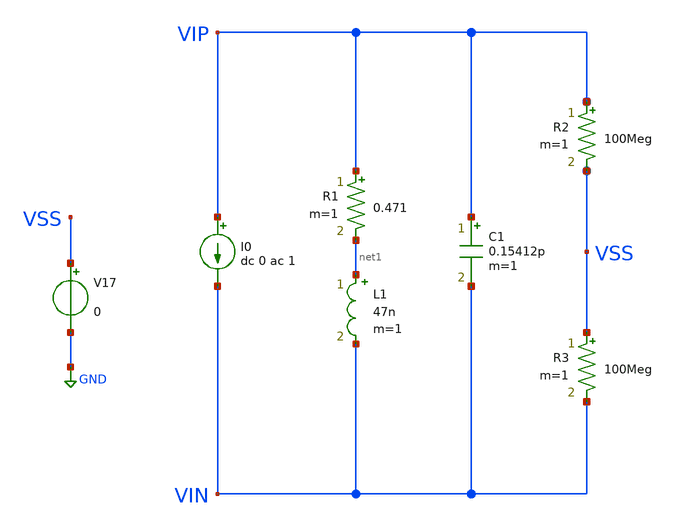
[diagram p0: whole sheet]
** sch_path: analog/tb/tb_coil_02.sch
**.subckt tb_coil_02
L1 net1 VIN 47n m=1
R1 VIP net1 0.471 m=1
C1 VIP VIN 0.15412p m=1
V17 VSS GND 0
R2 VIP VSS 100Meg m=1
R3 VSS VIN 100Meg m=1
I0 VIP VIN dc 0 ac 1
**** begin user architecture code



.save all
.save V(VIP) V(VIN) V(VIP, VIN)
.save I(VPORT)


.control
  set filetype=ascii        ; ASCII .raw (human-readable)
    run
    ac dec 1000 1Meg 1000Meg
    *tran 0.1u 100u
    let ZIN  = v(VIP, VIN)
    let ABSZ = abs(ZIN)
    let IMZ  = imag(ZIN)
    let REZ  = real(ZIN)
    let Q    = IMZ/REZ
    meas ac F_res when IMZ=0
    write tb_coil2.raw ABSZ Q abs(REZ)
    set appendwrite
.endc



.lib cornerMOSlv.lib mos_tt

**** end user architecture code
**.ends
.GLOBAL GND
.end
